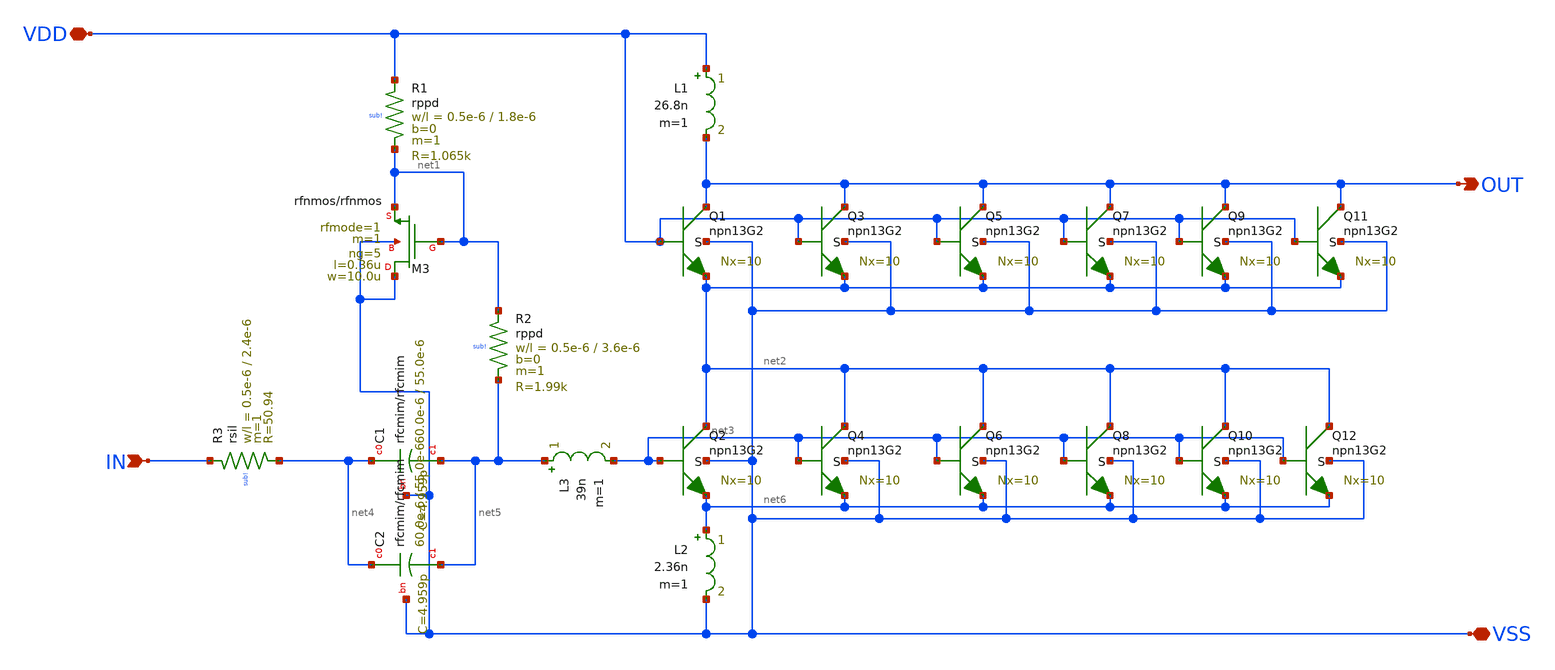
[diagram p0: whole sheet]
** sch_path: GPS_LNA/design_data/xschem/lna_full_base.sch
**.subckt lna_full_base VDD IN OUT VSS
*.iopin VDD
*.ipin IN
*.opin OUT
*.iopin VSS
XR2 net1 net5 sub! rppd w=0.5e-6 l=3.6e-6 m=1 b=0 mm_ok=1
XR1 VDD net1 sub! rppd w=0.5e-6 l=1.8e-6 m=1 b=0 mm_ok=1
XR3 IN net4 sub! rsil w=0.5e-6 l=2.4e-6 m=1 mm_ok=1
XC1 net4 net5 VSS rfcmim w=60.0e-6 l=55.0e-6 wfeed=5.0e-6 m=1 mm_ok=1
XC2 net4 net5 VSS rfcmim w=60.0e-6 l=55.0e-6 wfeed=5.0e-6 m=1 mm_ok=1
XM3 VSS net1 net1 VSS rfnmos w=10.0u l=0.36u ng=5 m=1 rfmode=1 mm_ok=1
XQ1 OUT VDD net2 VSS npn13G2 Nx=10 mm_ok=1
XQ2 net2 net3 net6 VSS npn13G2 Nx=10 mm_ok=1
XQ3 OUT VDD net2 VSS npn13G2 Nx=10 mm_ok=1
XQ4 net2 net3 net6 VSS npn13G2 Nx=10 mm_ok=1
XQ5 OUT VDD net2 VSS npn13G2 Nx=10 mm_ok=1
XQ6 net2 net3 net6 VSS npn13G2 Nx=10 mm_ok=1
XQ7 OUT VDD net2 VSS npn13G2 Nx=10 mm_ok=1
XQ8 net2 net3 net6 VSS npn13G2 Nx=10 mm_ok=1
XQ9 OUT VDD net2 VSS npn13G2 Nx=10 mm_ok=1
XQ10 net2 net3 net6 VSS npn13G2 Nx=10 mm_ok=1
XQ11 OUT VDD net2 VSS npn13G2 Nx=10 mm_ok=1
XQ12 net2 net3 net6 VSS npn13G2 Nx=10 mm_ok=1
L1 VDD OUT 26.8n m=1
L2 net6 VSS 2.36n m=1
L3 net5 net3 39n m=1
**.ends
.end
